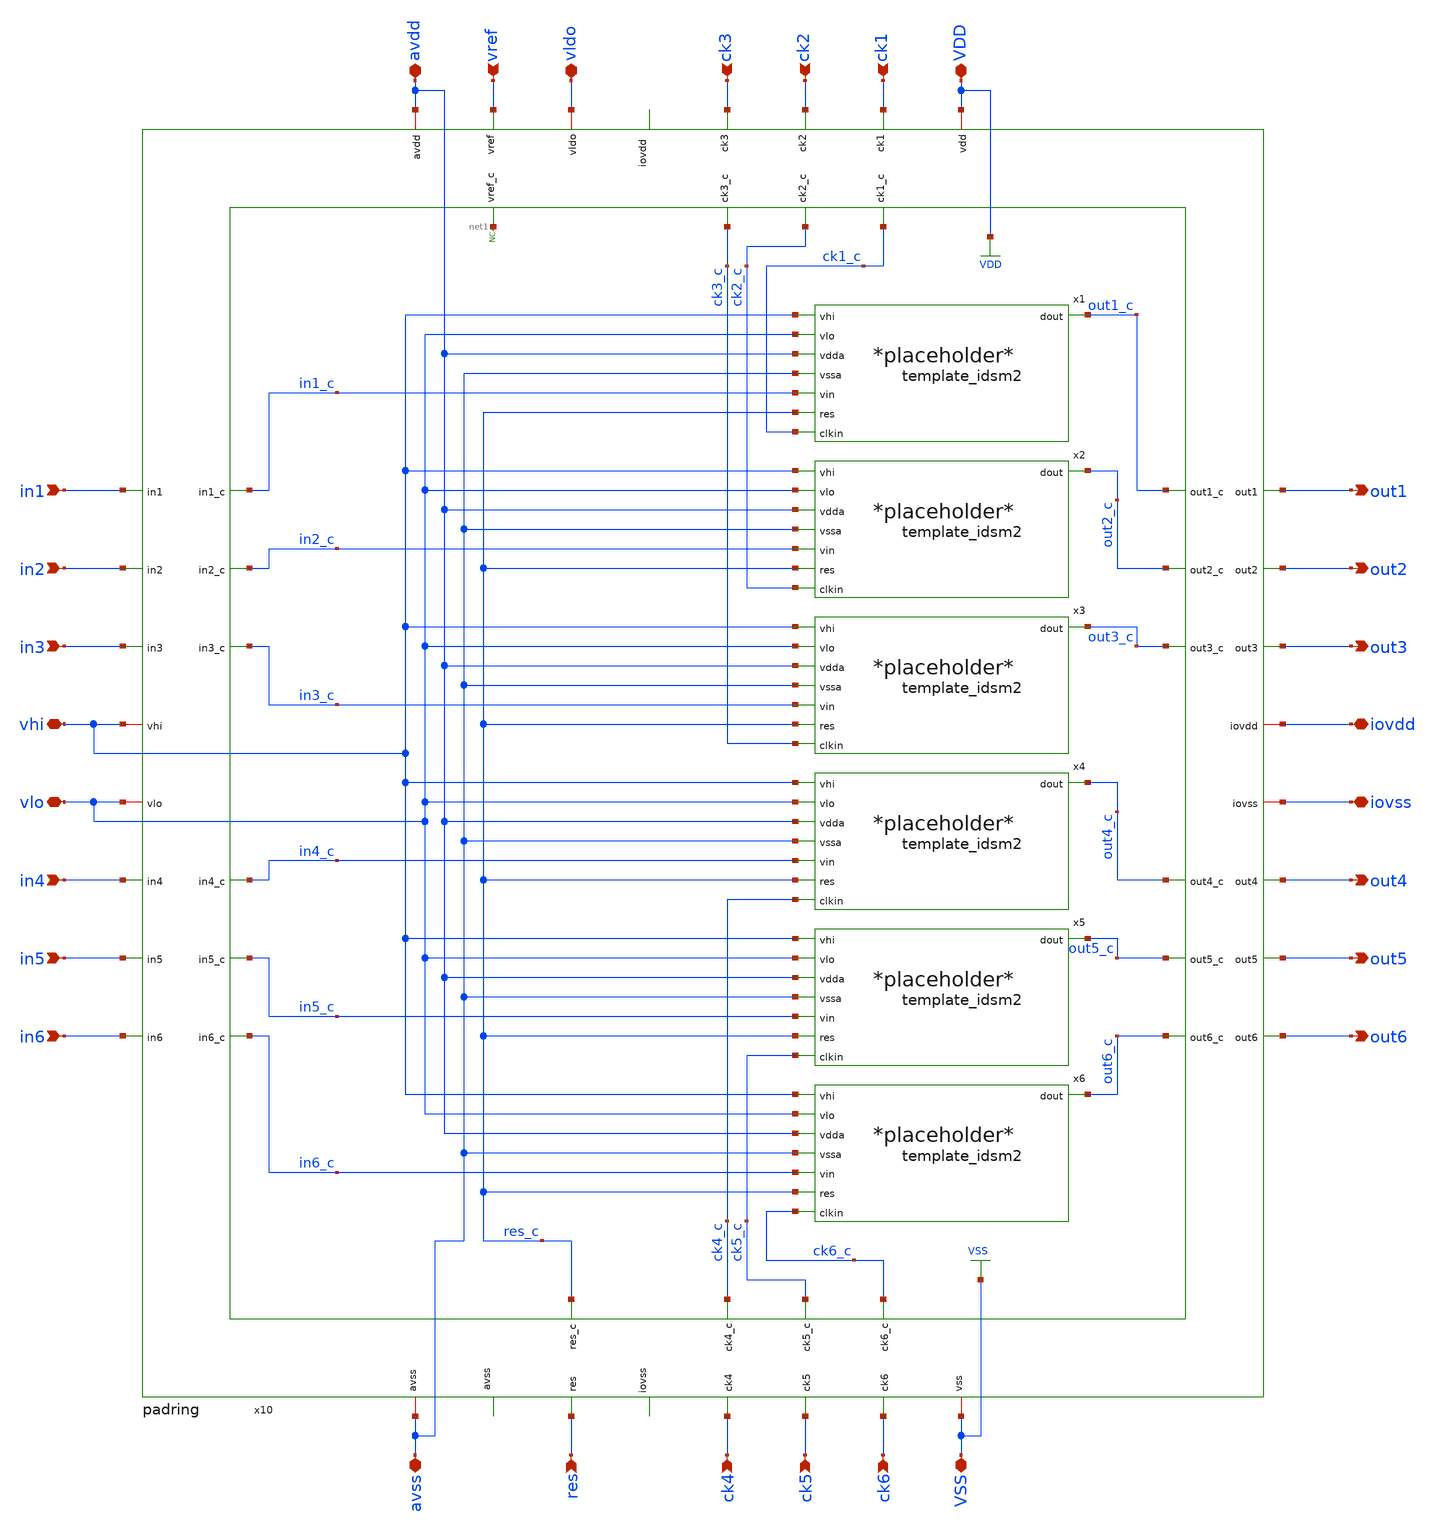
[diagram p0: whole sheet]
** sch_path: 5_Design/3_Real_circuits/UHEE628_S2024.sch
**.subckt UHEE628_S2024 in1 in2 in3 in4 in5 in6 iovdd vlo avss avdd out1 out2 out3 out4 out5 out6
*+ iovss VSS VDD vldo ck3 ck2 ck1 vref res ck4 ck5 ck6 vhi
*.ipin in1
*.ipin in2
*.ipin in3
*.ipin in4
*.ipin in5
*.ipin in6
*.iopin iovdd
*.iopin vlo
*.iopin avss
*.iopin avdd
*.opin out1
*.opin out2
*.opin out3
*.opin out4
*.opin out5
*.opin out6
*.iopin iovss
*.iopin VSS
*.iopin VDD
*.iopin vldo
*.ipin ck3
*.ipin ck2
*.ipin ck1
*.ipin vref
*.ipin res
*.ipin ck4
*.ipin ck5
*.ipin ck6
*.iopin vhi
x10 vref ck3 vldo ck1 ck2 ck1_c ck3_c net1 ck2_c out1_c in1 out1 in2 out2 out2_c in2_c VDD out3
+ in3_c in3 out3_c avdd iovdd vhi iovss avss vlo out4 in4_c in4 out4_c out5 in5_c out5_c in5 in6 in6_c out6
+ out6_c ck5_c ck4_c res_c ck6_c ck6 ck5 ck4 res in1_c VSS padring
x1 vhi vlo avdd avss in1_c out1_c res_c ck1_c template_idsm2
x2 vhi vlo avdd avss in2_c out2_c res_c ck2_c template_idsm2
x3 vhi vlo avdd avss in3_c out3_c res_c ck3_c template_idsm2
x4 vhi vlo avdd avss in4_c out4_c res_c ck4_c template_idsm2
x5 vhi vlo avdd avss in5_c out5_c res_c ck5_c template_idsm2
x6 vhi vlo avdd avss in6_c out6_c res_c ck6_c template_idsm2
* noconn #net1
**.ends
.GLOBAL VSS
.GLOBAL VDD
.end
